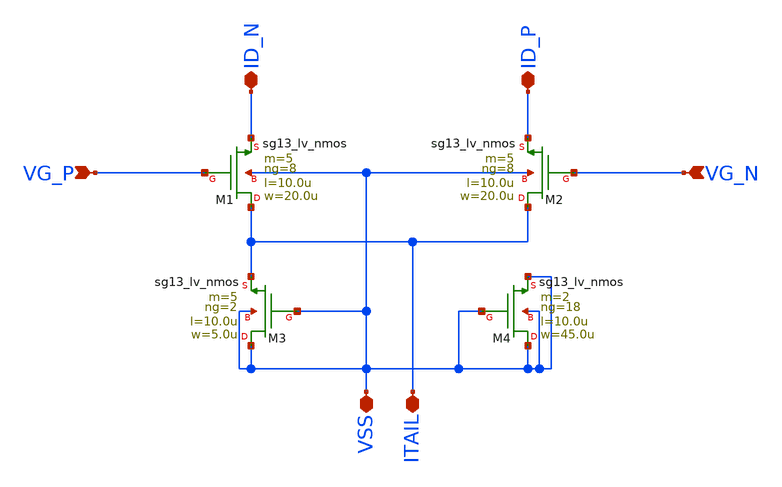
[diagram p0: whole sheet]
** sch_path: JKU_TC1/design_data/sfl-test-cells/xschem/diffpairs/dp_n_100u_10u.sch
**.subckt dp_n_100u_10u VG_P VG_N VSS ITAIL ID_N ID_P
*.ipin VG_P
*.ipin VG_N
*.iopin VSS
*.iopin ITAIL
*.iopin ID_N
*.iopin ID_P
XM1 ITAIL VG_P ID_N VSS sg13_lv_nmos w=20.0u l=10.0u ng=8 m=5 mm_ok=1
XM2 ITAIL VG_N ID_P VSS sg13_lv_nmos w=20.0u l=10.0u ng=8 m=5 mm_ok=1
XM3 VSS VSS ITAIL VSS sg13_lv_nmos w=5.0u l=10.0u ng=2 m=5 mm_ok=1
XM4 VSS VSS VSS VSS sg13_lv_nmos w=45.0u l=10.0u ng=18 m=2 mm_ok=1
**.ends
.end
